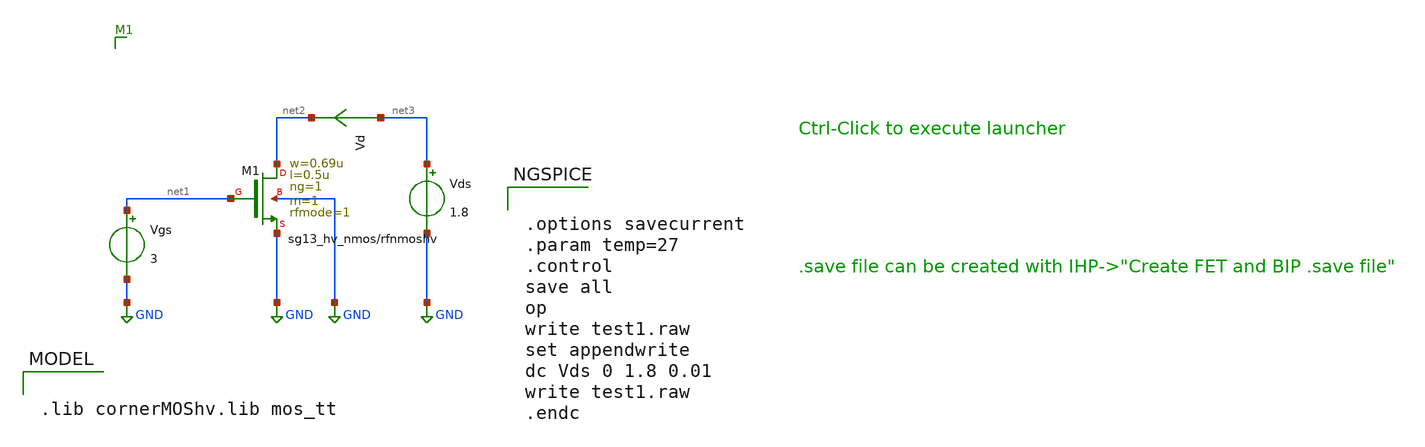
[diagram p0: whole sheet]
** sch_path: schematic/test1.sch
**.subckt test1
Vgs net1 GND 3
Vds net3 GND 1.8
Vd net3 net2 0
.save i(vd)
XM1 net2 net1 GND GND sg13_hv_nmos w=0.69u l=0.5u ng=1 m=1 rfmode=1 mm_ok=1
**** begin user architecture code

.lib cornerMOShv.lib mos_tt



.options savecurrent
.param temp=27
.control
save all
op
write test1.raw
set appendwrite
dc Vds 0 1.8 0.01
write test1.raw
.endc


**** end user architecture code
**.ends
.GLOBAL GND
.end
